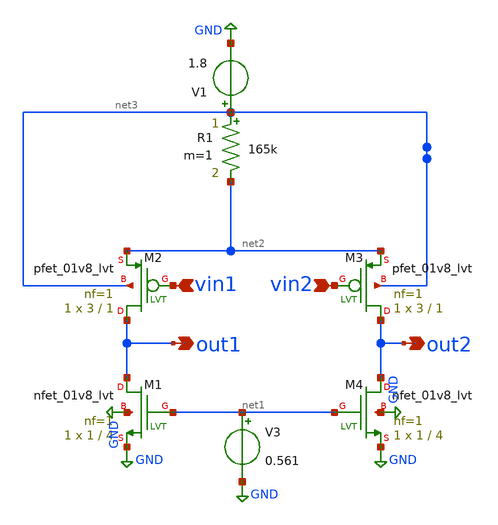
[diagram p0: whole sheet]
** sch_path: opampp.sch
**.subckt opampp out1 out2 vin1 vin2
*.opin out1
*.opin out2
*.ipin vin1
*.ipin vin2
XM1 out1 net1 GND GND sky130_fd_pr__nfet_01v8_lvt L=4 W=1 nf=1 ad='int((nf+1)/2) * W/nf * 0.29' as='int((nf+2)/2) * W/nf * 0.29'
+ pd='2*int((nf+1)/2) * (W/nf + 0.29)' ps='2*int((nf+2)/2) * (W/nf + 0.29)' nrd='0.29 / W' nrs='0.29 / W'
+ sa=0 sb=0 sd=0 mult=1 m=1
XM2 out1 vin1 net2 net3 sky130_fd_pr__pfet_01v8_lvt L=1 W=3 nf=1 ad='int((nf+1)/2) * W/nf * 0.29' as='int((nf+2)/2) * W/nf * 0.29'
+ pd='2*int((nf+1)/2) * (W/nf + 0.29)' ps='2*int((nf+2)/2) * (W/nf + 0.29)' nrd='0.29 / W' nrs='0.29 / W'
+ sa=0 sb=0 sd=0 mult=1 m=1
XM3 out2 vin2 net2 net3 sky130_fd_pr__pfet_01v8_lvt L=1 W=3 nf=1 ad='int((nf+1)/2) * W/nf * 0.29' as='int((nf+2)/2) * W/nf * 0.29'
+ pd='2*int((nf+1)/2) * (W/nf + 0.29)' ps='2*int((nf+2)/2) * (W/nf + 0.29)' nrd='0.29 / W' nrs='0.29 / W'
+ sa=0 sb=0 sd=0 mult=1 m=1
XM4 out2 net1 GND GND sky130_fd_pr__nfet_01v8_lvt L=4 W=1 nf=1 ad='int((nf+1)/2) * W/nf * 0.29' as='int((nf+2)/2) * W/nf * 0.29'
+ pd='2*int((nf+1)/2) * (W/nf + 0.29)' ps='2*int((nf+2)/2) * (W/nf + 0.29)' nrd='0.29 / W' nrs='0.29 / W'
+ sa=0 sb=0 sd=0 mult=1 m=1
V1 net3 GND 1.8
V3 net1 GND 0.561
R1 net3 net2 165k m=1
**.ends
.GLOBAL GND
.end
